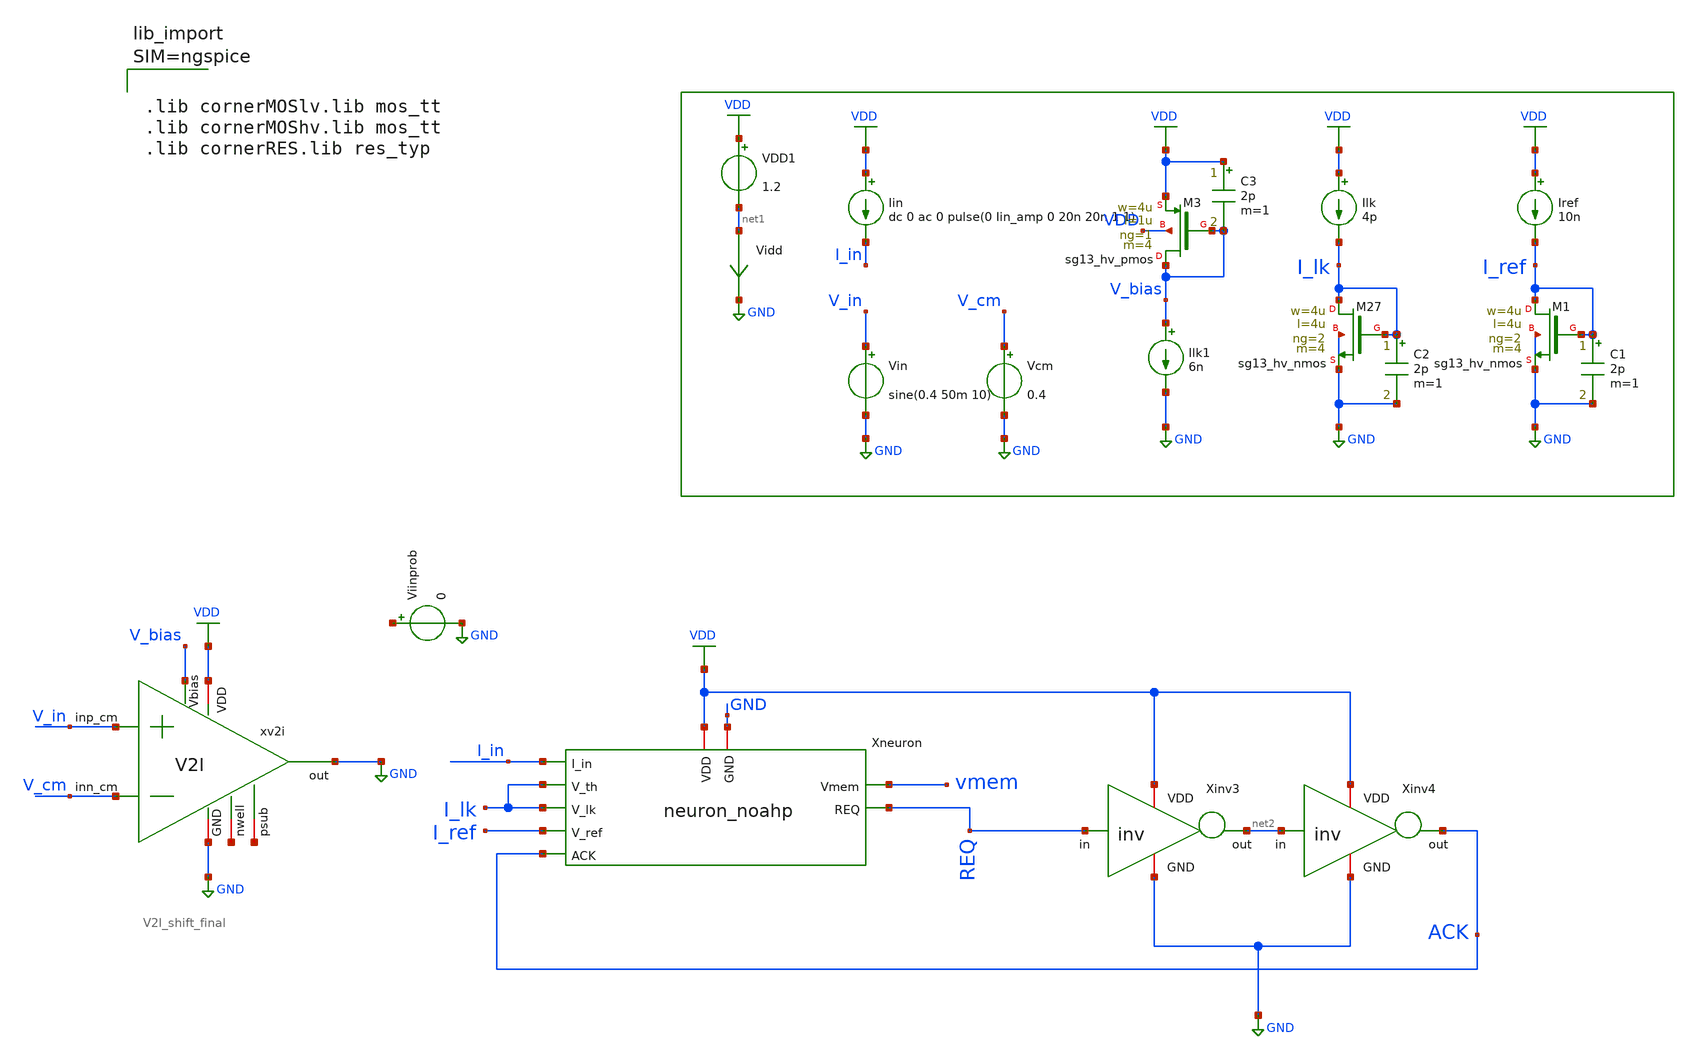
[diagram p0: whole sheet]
** sch_path: xschem/neuron_noahp_tb.sch
**.subckt neuron_noahp_tb
Xneuron VDD I_in I_lk I_lk vmem REQ ACK I_ref GND neuron_noahp
Ilk VDD I_lk 4p
Iin VDD I_in dc 0 ac 0 pulse(0 Iin_amp 0 20n 20n 1 1)
VDD1 VDD net1 1.2
Iref VDD I_ref 10n
Vidd net1 GND 0
.save i(vidd)
XM27 I_lk I_lk GND GND sg13_hv_nmos w=4u l=4u ng=2 m=4 mm_ok=1
Xinv3 VDD REQ net2 GND inv
Xinv4 VDD net2 ACK GND inv
C2 I_lk GND 2p m=1
XM1 I_ref I_ref GND GND sg13_hv_nmos w=4u l=4u ng=2 m=4 mm_ok=1
C1 I_ref GND 2p m=1
xv2i VDD V_bias V_cm V_in GND GND net3 net4 V2I_shift_final
XM3 V_bias V_bias VDD VDD sg13_hv_pmos w=4u l=1u ng=1 m=4 mm_ok=1
C3 VDD V_bias 2p m=1
Ilk1 V_bias GND 6n
Vcm V_cm GND 0.4
Vin V_in GND sine(0.4 50m 10)
Viinprob net5 GND 0
.save i(viinprob)
**** begin user architecture code



.param temp=27
.param Iin_amp=4n

.ic V(vmem)=0 V(xneuron.xref.vref)=0 V(REQ)=1.2 V(ACK)=1.2

.options gmin=1e-13
.control

save V(I_lk) V(I_in) I(Viinprob)
save V(ACK) V(REQ) V(vmem) V(xneuron.xref.vref)
save V(xneuron.xfb.vmir) V(xneuron.vfb)
save V(xneuron.xfb.nwell) V(xneuron.xfb.psub)
save V(V_in) V(V_cm) V(xv2i.vhead)


tran 50n 20m
write neuron_noahp_tb.raw
.endc







.lib cornerMOSlv.lib mos_tt
.lib cornerMOShv.lib mos_tt
.lib cornerRES.lib res_typ


**** end user architecture code
**.ends
.GLOBAL GND
.GLOBAL VDD
.end
